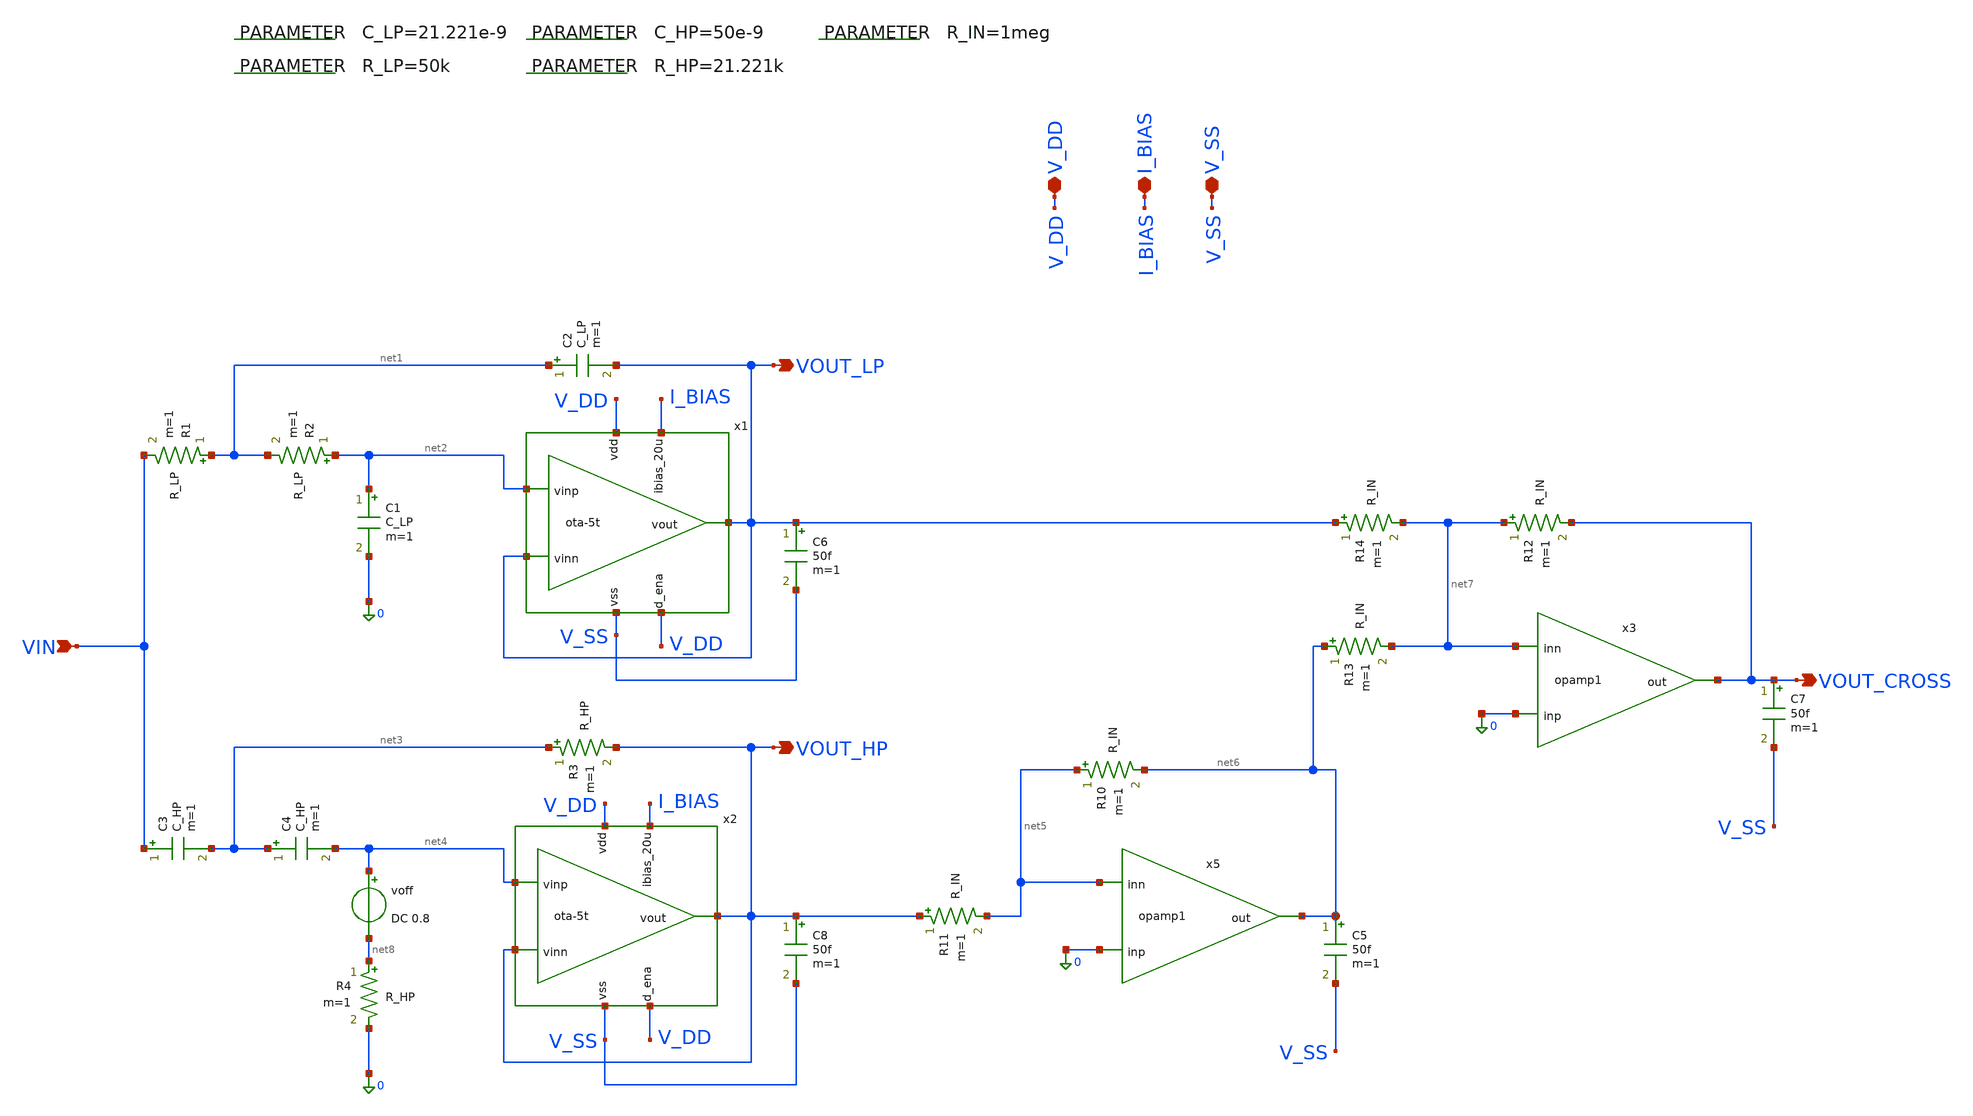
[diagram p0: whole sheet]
** sch_path: 004_Real_Circuits/001_version_basic_ota_pretl/linkwtz_riley_crossover_pretl_OTA.sch
* 004_Real_Circuits/001_version_basic_ota_pretl/ota-5t.sch:
* (c) 2024-2025 Harald Pretl, Apache-2.0 license
**.subckt linkwtz_riley_crossover_pretl_OTA VOUT_LP VOUT_HP VIN VOUT_CROSS V_DD I_BIAS V_SS
*.opin VOUT_LP
*.opin VOUT_HP
*.ipin VIN
*.opin VOUT_CROSS
*.iopin V_DD
*.iopin I_BIAS
*.iopin V_SS
R1 net1 VIN R_LP m=1
R2 net2 net1 R_LP m=1
C1 net2 0 C_LP m=1
C2 net1 VOUT_LP C_LP m=1
C3 VIN net3 C_HP m=1
C4 net3 net4 C_HP m=1
R3 net3 VOUT_HP R_HP m=1
R4 net8 0 R_HP m=1
R10 net5 net6 R_IN m=1
R11 VOUT_HP net5 R_IN m=1
R12 net7 VOUT_CROSS R_IN m=1
R13 net6 net7 R_IN m=1
R14 VOUT_LP net7 R_IN m=1
x1 V_DD VOUT_LP net2 VOUT_LP I_BIAS V_DD V_SS ota-5t
x2 V_DD VOUT_HP net4 VOUT_HP I_BIAS V_DD V_SS ota-5t
C8 VOUT_HP V_SS 50f m=1
C5 net6 V_SS 50f m=1
C6 VOUT_LP V_SS 50f m=1
C7 VOUT_CROSS V_SS 50f m=1
.param R_IN=1meg
.param C_LP=21.221e-9
.param R_LP=50k
.param C_HP=50e-9
.param R_HP=21.221k
voff net4 net8 DC 0.8
x5 0 net5 net6 opamp1
x3 0 net7 VOUT_CROSS opamp1
**.ends

* expanding   symbol:  004_Real_Circuits/001_version_basic_ota_pretl/ota-5t.sym # of pins=7
** sym_path: 004_Real_Circuits/001_version_basic_ota_pretl/ota-5t.sym
** sch_path: 004_Real_Circuits/001_version_basic_ota_pretl/ota-5t.sch
.subckt ota-5t vdd vout vinp vinn ibias_20u d_ena vss
*.ipin ibias_20u
*.iopin vdd
*.iopin vss
*.ipin vinp
*.ipin vinn
*.opin vout
*.ipin d_ena
XM5 tail gate_n vss vss sg13_lv_nmos w=1.5u l=5u ng=1 m=1 mm_ok=1
XM4 vout gate_p vdd vdd sg13_lv_pmos w=3.5u l=5u ng=1 m=1 mm_ok=1
XM1 gate_p vinp tail vss sg13_lv_nmos w=2u l=5u ng=1 m=1 mm_ok=1
XM2 vout vinn tail vss sg13_lv_nmos w=2u l=5u ng=1 m=1 mm_ok=1
XM3 gate_p gate_p vdd vdd sg13_lv_pmos w=3.5u l=5u ng=1 m=1 mm_ok=1
XM6 ibias_20u gate_n vss vss sg13_lv_nmos w=10u l=5u ng=5 m=1 mm_ok=1
XM9 gate_n ena_n vss vss sg13_lv_nmos w=0.5u l=0.13u ng=1 m=1 mm_ok=1
XM11 gate_p ena vdd vdd sg13_lv_pmos w=1.5u l=0.13u ng=1 m=1 mm_ok=1
XM7 ena ena_n vss vss sg13_lv_nmos w=0.5u l=0.13u ng=1 m=1 mm_ok=1
XM8 ena ena_n vdd vdd sg13_lv_pmos w=1.5u l=0.13u ng=1 m=1 mm_ok=1
XM10 ibias_20u ena gate_n vss sg13_lv_nmos w=0.5u l=0.13u ng=1 m=1 mm_ok=1
XM12 ena_n d_ena vss vss sg13_lv_nmos w=0.5u l=0.13u ng=1 m=1 mm_ok=1
XM13 ena_n d_ena vdd vdd sg13_lv_pmos w=1.5u l=0.13u ng=1 m=1 mm_ok=1
.ends


* expanding   symbol:  001_provided_files/2_Idealized_circuits/opamp1.sym # of pins=3
** sym_path: 001_provided_files/2_Idealized_circuits/opamp1.sym
** sch_path: 001_provided_files/2_Idealized_circuits/opamp1.sch
.subckt opamp1 inp inn out
*.ipin inp
*.ipin inn
*.opin out
Rin inp inn 10MEG m=1
Rout net2 out 10 m=1
Cp net1 GND 1.59u m=1
Rp GND net1 1k m=1
Ebuf net2 GND net1 GND 1
G1 net1 GND inp inn 1
.ends

.GLOBAL GND
.end
